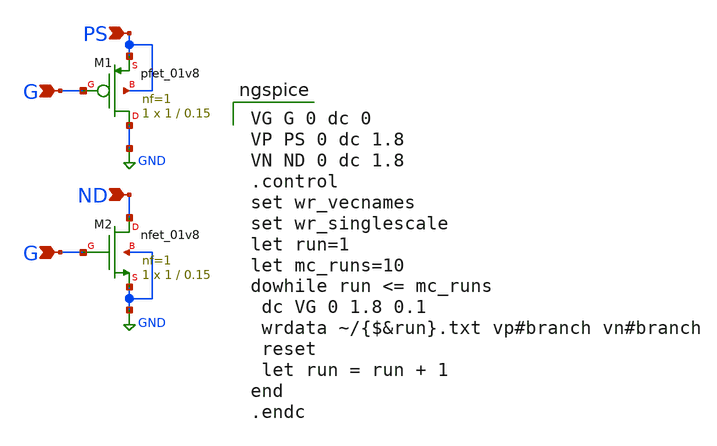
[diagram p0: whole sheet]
** sch_path: trbench_mc.sch
**.subckt trbench_mc ND PS G G
*.ipin ND
*.ipin PS
*.ipin G
*.ipin G
XM1 GND G PS PS sky130_fd_pr__pfet_01v8 L=0.15 W=1 nf=1 ad='int((nf+1)/2) * W/nf * 0.29' as='int((nf+2)/2) * W/nf * 0.29'
+ pd='2*int((nf+1)/2) * (W/nf + 0.29)' ps='2*int((nf+2)/2) * (W/nf + 0.29)' nrd='0.29 / W' nrs='0.29 / W'
+ sa=0 sb=0 sd=0 mult=1 m=1
XM2 ND G GND GND sky130_fd_pr__nfet_01v8 L=0.15 W=1 nf=1 ad='int((nf+1)/2) * W/nf * 0.29' as='int((nf+2)/2) * W/nf * 0.29'
+ pd='2*int((nf+1)/2) * (W/nf + 0.29)' ps='2*int((nf+2)/2) * (W/nf + 0.29)' nrd='0.29 / W' nrs='0.29 / W'
+ sa=0 sb=0 sd=0 mult=1 m=1
**** begin user architecture code

VG G 0 dc 0
VP PS 0 dc 1.8
VN ND 0 dc 1.8
.control
set wr_vecnames
set wr_singlescale
let run=1
let mc_runs=10
dowhile run <= mc_runs
 dc VG 0 1.8 0.1
 wrdata ~/{$&run}.txt vp#branch vn#branch
 reset
 let run = run + 1
end
.endc


** opencircuitdesign pdks install
.lib $::SKYWATER_MODELS/sky130.lib.spice mc


**** end user architecture code
**.ends
.GLOBAL GND
.end
